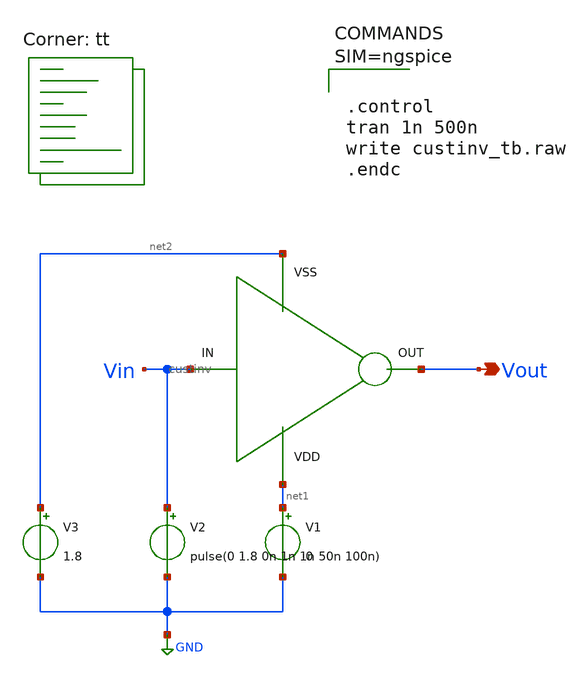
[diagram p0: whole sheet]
** sch_path: xschem/custinv_tb.sch
**.subckt custinv_tb Vout
*.opin Vout
X1 net2 net1 Vout Vin custinv
V1 net1 GND 0
V2 Vin GND pulse(0 1.8 0n 1n 1n 50n 100n)
V3 net2 GND 1.8
**** begin user architecture code



.control
tran 1n 500n
write custinv_tb.raw
.endc



.lib $::SKYWATER_MODELS/sky130.lib.spice tt
**** end user architecture code
**.ends

* expanding   symbol:  custinv.sym # of pins=4
** sym_path: xschem/custinv.sym
** sch_path: xschem/custinv.sch
.subckt custinv VSS VDD OUT IN
*.ipin IN
*.opin OUT
*.iopin VSS
*.iopin VDD
XM1 OUT IN VDD VDD sky130_fd_pr__nfet_01v8 L=0.15 W=1 nf=1 ad='int((nf+1)/2) * W/nf * 0.29' as='int((nf+2)/2) * W/nf * 0.29'
+ pd='2*int((nf+1)/2) * (W/nf + 0.29)' ps='2*int((nf+2)/2) * (W/nf + 0.29)' nrd='0.29 / W' nrs='0.29 / W'
+ sa=0 sb=0 sd=0 mult=1 m=1
XM2 OUT IN VSS VSS sky130_fd_pr__pfet_01v8 L=0.15 W=1 nf=1 ad='int((nf+1)/2) * W/nf * 0.29' as='int((nf+2)/2) * W/nf * 0.29'
+ pd='2*int((nf+1)/2) * (W/nf + 0.29)' ps='2*int((nf+2)/2) * (W/nf + 0.29)' nrd='0.29 / W' nrs='0.29 / W'
+ sa=0 sb=0 sd=0 mult=1 m=1
.ends

.GLOBAL GND
.end
